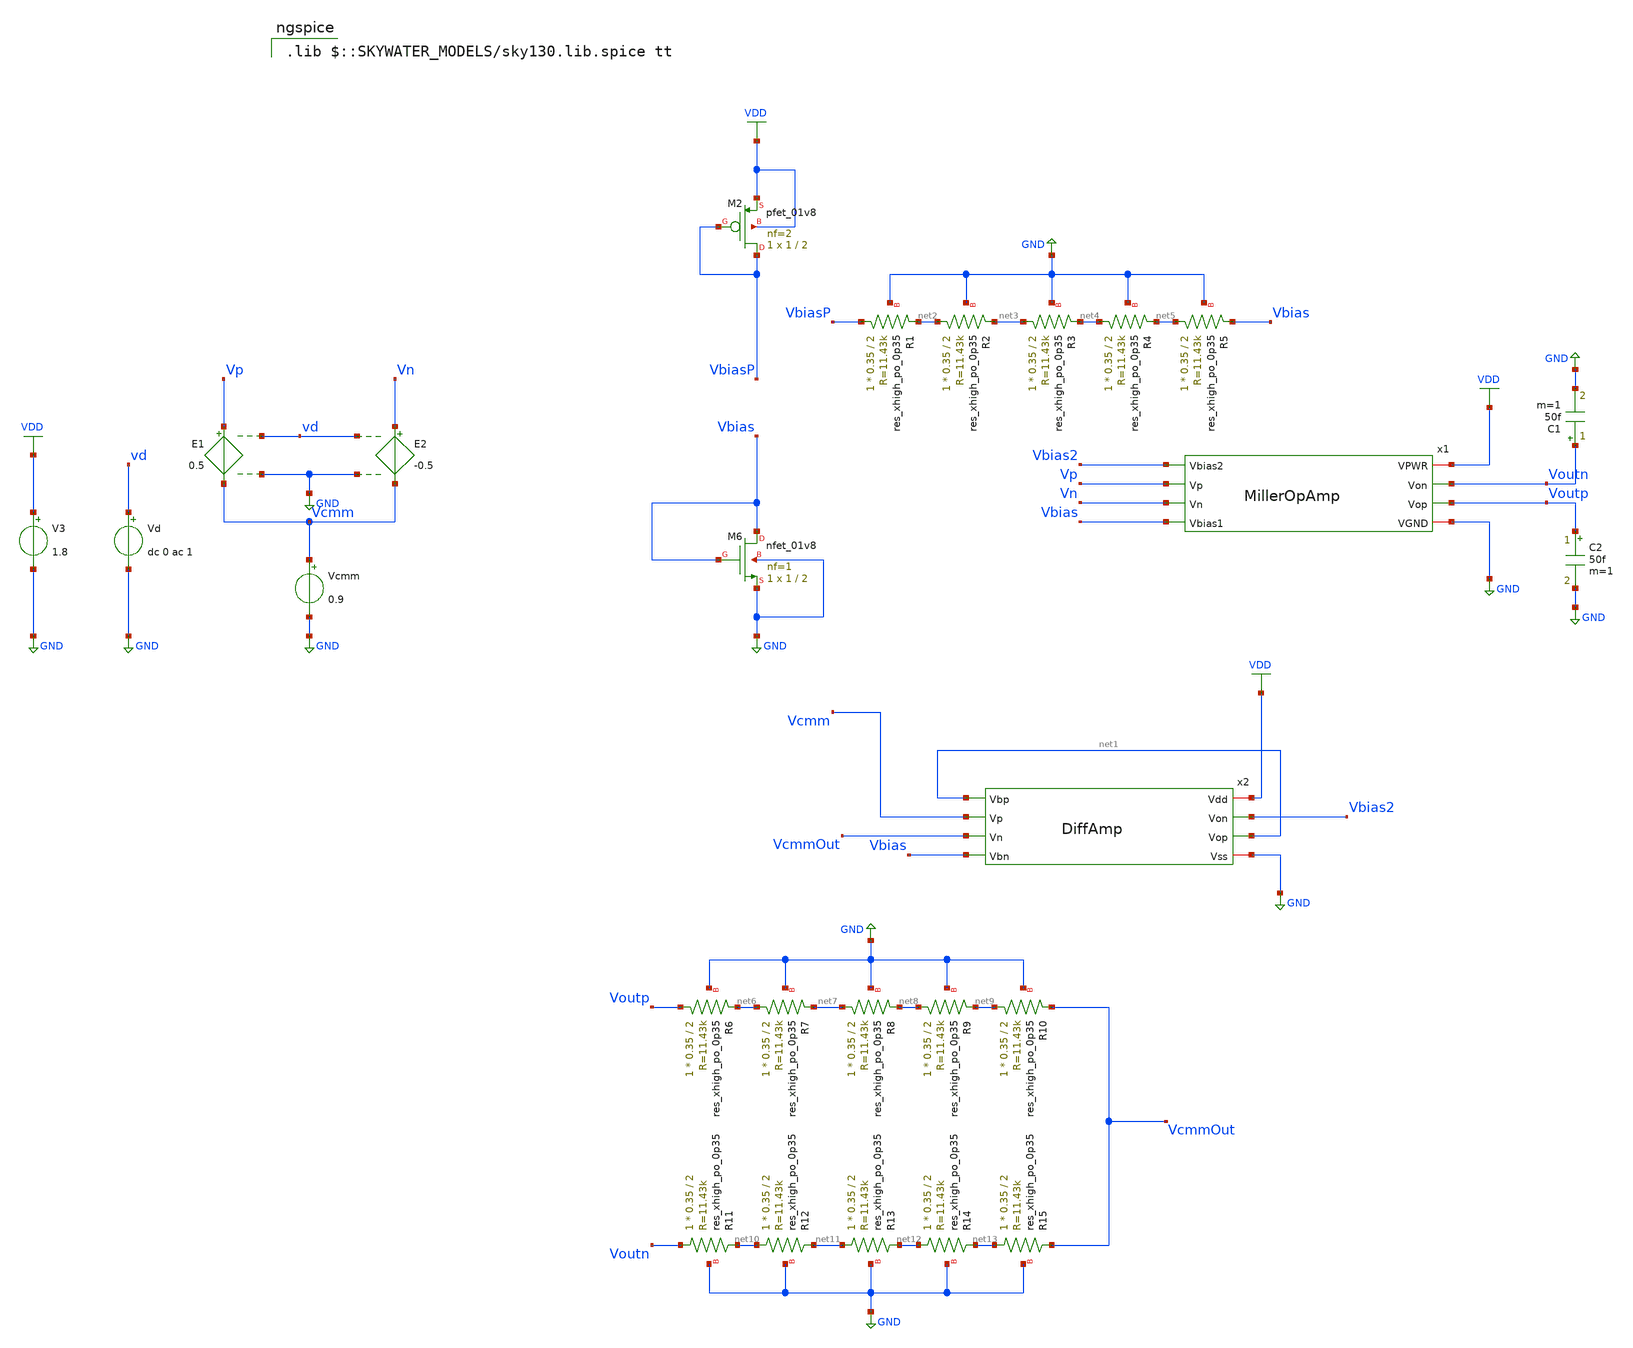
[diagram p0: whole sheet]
** sch_path: Circuits/Examples/MillerOpAmpCMMFB/MillerOpAmp_tb.sch
**.subckt MillerOpAmp_tb
V3 VDD GND 1.8
E1 Vp Vcmm vd GND 0.5
E2 Vn Vcmm vd GND -0.5
Vcmm Vcmm GND 0.9
Vd vd GND dc 0 ac 1
XM6 Vbias Vbias GND GND sky130_fd_pr__nfet_01v8 L=2 W=1 nf=1 ad='int((nf+1)/2) * W/nf * 0.29' as='int((nf+2)/2) * W/nf * 0.29'
+ pd='2*int((nf+1)/2) * (W/nf + 0.29)' ps='2*int((nf+2)/2) * (W/nf + 0.29)' nrd='0.29 / W' nrs='0.29 / W'
+ sa=0 sb=0 sd=0 mult=1 m=1
x1 VDD Voutn Vbias2 Vp Vn Vbias Voutp GND MillerOpAmp
C2 Voutp GND 50f m=1
C1 Voutn GND 50f m=1
x2 VDD net1 Vbias2 net1 Vcmm VcmmOut Vbias GND DiffAmp
XM2 VbiasP VbiasP VDD VDD sky130_fd_pr__pfet_01v8 L=2 W=1 nf=2 ad='int((nf+1)/2) * W/nf * 0.29' as='int((nf+2)/2) * W/nf * 0.29'
+ pd='2*int((nf+1)/2) * (W/nf + 0.29)' ps='2*int((nf+2)/2) * (W/nf + 0.29)' nrd='0.29 / W' nrs='0.29 / W'
+ sa=0 sb=0 sd=0 mult=1 m=1
XR1 VbiasP net2 GND sky130_fd_pr__res_xhigh_po_0p35 L=2 mult=1 m=1
XR2 net2 net3 GND sky130_fd_pr__res_xhigh_po_0p35 L=2 mult=1 m=1
XR3 net3 net4 GND sky130_fd_pr__res_xhigh_po_0p35 L=2 mult=1 m=1
XR4 net4 net5 GND sky130_fd_pr__res_xhigh_po_0p35 L=2 mult=1 m=1
XR5 net5 Vbias GND sky130_fd_pr__res_xhigh_po_0p35 L=2 mult=1 m=1
XR6 Voutp net6 GND sky130_fd_pr__res_xhigh_po_0p35 L=2 mult=1 m=1
XR7 net6 net7 GND sky130_fd_pr__res_xhigh_po_0p35 L=2 mult=1 m=1
XR8 net7 net8 GND sky130_fd_pr__res_xhigh_po_0p35 L=2 mult=1 m=1
XR9 net8 net9 GND sky130_fd_pr__res_xhigh_po_0p35 L=2 mult=1 m=1
XR10 net9 VcmmOut GND sky130_fd_pr__res_xhigh_po_0p35 L=2 mult=1 m=1
XR11 Voutn net10 GND sky130_fd_pr__res_xhigh_po_0p35 L=2 mult=1 m=1
XR12 net10 net11 GND sky130_fd_pr__res_xhigh_po_0p35 L=2 mult=1 m=1
XR13 net11 net12 GND sky130_fd_pr__res_xhigh_po_0p35 L=2 mult=1 m=1
XR14 net12 net13 GND sky130_fd_pr__res_xhigh_po_0p35 L=2 mult=1 m=1
XR15 net13 VcmmOut GND sky130_fd_pr__res_xhigh_po_0p35 L=2 mult=1 m=1
**** begin user architecture code



* ngspice commands
.option savecurrents
.save all
.control
ac dec 1001 1 100Meg
let vod = V(Voutp)-V(Voutn)
meas ac gain max vod
let gain3dB = gain/sqrt(2)
meas ac BW TRIG at=1 TARG vod val=gain3dB fall=LAST
let GBW = BW*gain*1e-6
print GBW
print vodmax
plot vdb(vod) xlimit 1k 100Meg ylabel 'small signal gain'
let outd = 180/PI*cph(vod)
meas ac ftHz when vdb(vod)=1 fall=LAST
meas ac ph find outd when vdb(vod)=0 fall=LAST
let phm = ph+180
print phm
settype phase outd
plot outd xlimit 1k 100Meg ylabel 'phase'
dc Vd -0.02 0.02 1m
let vod = V(Voutp)-V(Voutn)
plot vod
op
write MillerOpAmp_tb.raw
.endc



 .lib $::SKYWATER_MODELS/sky130.lib.spice tt

**** end user architecture code
**.ends

* expanding   symbol:  /foss/designs/xschem/MillerOpAmp/MillerOpAmp.sym # of pins=8
** sym_path: Circuits/MillerOpAmp/MillerOpAmp.sym
** sch_path: Circuits/MillerOpAmp/MillerOpAmp.sch
.subckt MillerOpAmp VPWR Von Vbias2 Vp Vn Vbias1 Vop VGND
*.opin Von
*.opin Vop
*.ipin Vbias2
*.ipin Vp
*.ipin Vn
*.ipin Vbias1
*.iopin VPWR
*.iopin VGND
x1 VPWR Vbias2 Von1 Vop1 Vp Vn Vbias1 VGND DiffAmp
x2 VPWR Von1 Von Vbias1 VGND CSAmp
x3 VPWR Vop1 Vop Vbias1 VGND CSAmp
XC1 Von1 Von sky130_fd_pr__cap_mim_m3_1 W=5 L=5 MF=1 m=1
XC2 Vop1 Vop sky130_fd_pr__cap_mim_m3_1 W=5 L=5 MF=1 m=1
.ends


* expanding   symbol:  /foss/designs/xschem/MillerOpAmp/DiffAmp.sym # of pins=8
** sym_path: Circuits/Examples/OpAmp/DiffAmp.sym
** sch_path: Circuits/Examples/OpAmp/DiffAmp.sch
.subckt DiffAmp Vdd Vbp Von Vop Vp Vn Vbn Vss
*.iopin Vdd
*.iopin Vss
*.ipin Vp
*.ipin Vn
*.ipin Vbn
*.ipin Vbp
*.opin Vop
*.opin Von
XM1 Vop Vp vmid Vss sky130_fd_pr__nfet_01v8 L=1 W=1 nf=1 ad='int((nf+1)/2) * W/nf * 0.29' as='int((nf+2)/2) * W/nf * 0.29'
+ pd='2*int((nf+1)/2) * (W/nf + 0.29)' ps='2*int((nf+2)/2) * (W/nf + 0.29)' nrd='0.29 / W' nrs='0.29 / W'
+ sa=0 sb=0 sd=0 mult=1 m=1
XM2 Von Vn vmid Vss sky130_fd_pr__nfet_01v8 L=1 W=1 nf=1 ad='int((nf+1)/2) * W/nf * 0.29' as='int((nf+2)/2) * W/nf * 0.29'
+ pd='2*int((nf+1)/2) * (W/nf + 0.29)' ps='2*int((nf+2)/2) * (W/nf + 0.29)' nrd='0.29 / W' nrs='0.29 / W'
+ sa=0 sb=0 sd=0 mult=1 m=1
XM3 Vop Vbp Vdd Vdd sky130_fd_pr__pfet_01v8 L=1 W=2 nf=1 ad='int((nf+1)/2) * W/nf * 0.29' as='int((nf+2)/2) * W/nf * 0.29'
+ pd='2*int((nf+1)/2) * (W/nf + 0.29)' ps='2*int((nf+2)/2) * (W/nf + 0.29)' nrd='0.29 / W' nrs='0.29 / W'
+ sa=0 sb=0 sd=0 mult=1 m=1
XM4 Von Vbp Vdd Vdd sky130_fd_pr__pfet_01v8 L=1 W=2 nf=1 ad='int((nf+1)/2) * W/nf * 0.29' as='int((nf+2)/2) * W/nf * 0.29'
+ pd='2*int((nf+1)/2) * (W/nf + 0.29)' ps='2*int((nf+2)/2) * (W/nf + 0.29)' nrd='0.29 / W' nrs='0.29 / W'
+ sa=0 sb=0 sd=0 mult=1 m=1
XM5 vmid Vbn Vss Vss sky130_fd_pr__nfet_01v8 L=2 W=1 nf=1 ad='int((nf+1)/2) * W/nf * 0.29' as='int((nf+2)/2) * W/nf * 0.29'
+ pd='2*int((nf+1)/2) * (W/nf + 0.29)' ps='2*int((nf+2)/2) * (W/nf + 0.29)' nrd='0.29 / W' nrs='0.29 / W'
+ sa=0 sb=0 sd=0 mult=1 m=1
.ends


* expanding   symbol:
*+  /home/jakob/Documents/AutomatedLayoutGeneration/Circuits/MillerOpAmp/CSAmp.sym # of pins=5
** sym_path: Circuits/MillerOpAmp/CSAmp.sym
** sch_path: Circuits/MillerOpAmp/CSAmp.sch
.subckt CSAmp Vdd Vi Vo Vbias1 Vss
*.ipin Vbias1
*.ipin Vi
*.iopin Vdd
*.iopin Vss
*.opin Vo
XM1 Vo Vi Vdd Vdd sky130_fd_pr__pfet_01v8 L=1 W=4 nf=2 ad='int((nf+1)/2) * W/nf * 0.29' as='int((nf+2)/2) * W/nf * 0.29'
+ pd='2*int((nf+1)/2) * (W/nf + 0.29)' ps='2*int((nf+2)/2) * (W/nf + 0.29)' nrd='0.29 / W' nrs='0.29 / W'
+ sa=0 sb=0 sd=0 mult=1 m=1
XM2 Vo Vbias1 Vss Vss sky130_fd_pr__nfet_01v8 L=2 W=8 nf=4 ad='int((nf+1)/2) * W/nf * 0.29' as='int((nf+2)/2) * W/nf * 0.29'
+ pd='2*int((nf+1)/2) * (W/nf + 0.29)' ps='2*int((nf+2)/2) * (W/nf + 0.29)' nrd='0.29 / W' nrs='0.29 / W'
+ sa=0 sb=0 sd=0 mult=1 m=1
.ends

.GLOBAL GND
.GLOBAL VDD
.end
